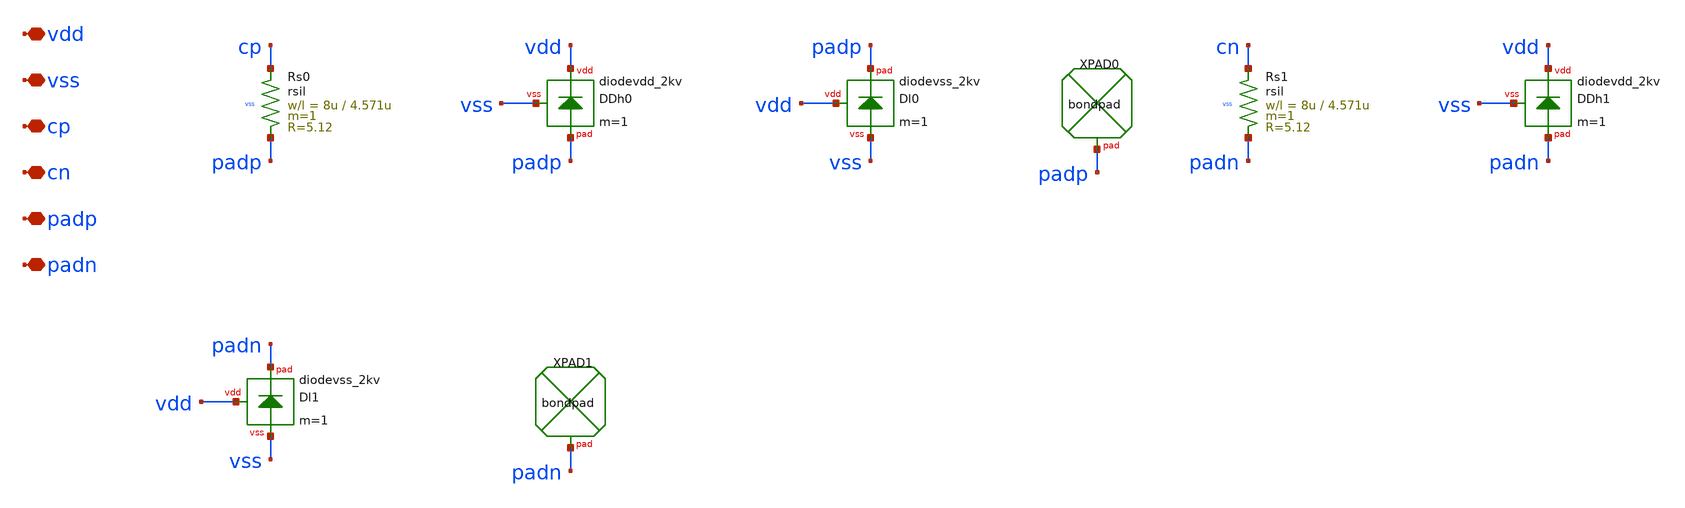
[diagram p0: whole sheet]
** sch_path: design/tx/pad_esd.sch
**.subckt pad_esd vdd vss cp cn padp padn
*.iopin vdd
*.iopin vss
*.iopin cp
*.iopin cn
*.iopin padp
*.iopin padn
XRs0 cp padp vss rsil w=8u l=4.571u m=1 mm_ok=1
XDh0 vdd padp vss diodevdd_2kv m=1
XDl0 vdd padp vss diodevss_2kv m=1
XXPAD0 padp bondpad size=80u shape=0 padtype=0
XRs1 cn padn vss rsil w=8u l=4.571u m=1 mm_ok=1
XDh1 vdd padn vss diodevdd_2kv m=1
XDl1 vdd padn vss diodevss_2kv m=1
XXPAD1 padn bondpad size=80u shape=0 padtype=0
**.ends
.end
